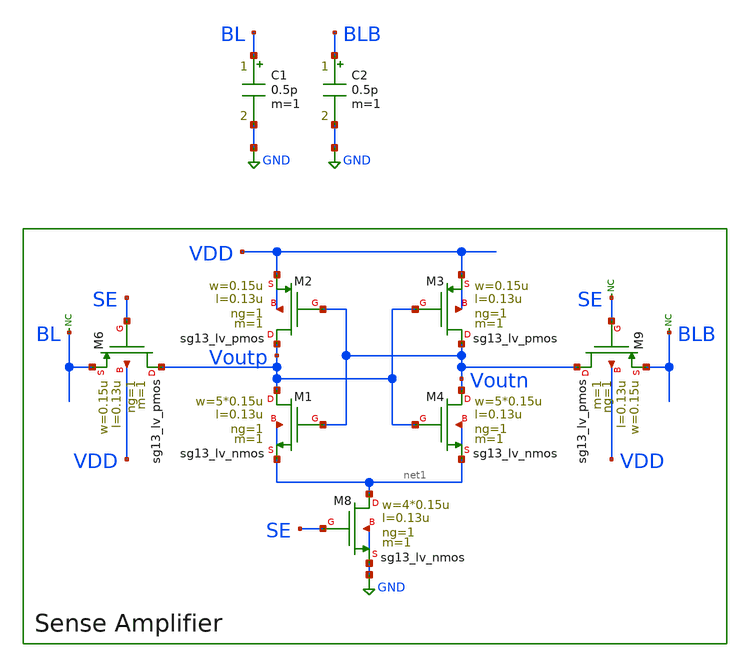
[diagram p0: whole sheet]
** sch_path: xschem/offset_voltage_tester/offset-voltage-tester.sch
**.subckt offset-voltage-tester
XM8 net1 SE GND GND sg13_lv_nmos w=4*0.15u l=0.13u ng=1 m=1 mm_ok=1
XM1 Voutp Voutn net1 net1 sg13_lv_nmos w=5*0.15u l=0.13u ng=1 m=1 mm_ok=1
XM3 Voutn Voutp VDD VDD sg13_lv_pmos w=0.15u l=0.13u ng=1 m=1 mm_ok=1
XM2 Voutp Voutn VDD VDD sg13_lv_pmos w=0.15u l=0.13u ng=1 m=1 mm_ok=1
XM4 Voutn Voutp net1 net1 sg13_lv_nmos w=5*0.15u l=0.13u ng=1 m=1 mm_ok=1
XM6 Voutp SE BL VDD sg13_lv_pmos w=0.15u l=0.13u ng=1 m=1 mm_ok=1
XM9 Voutn SE BLB VDD sg13_lv_pmos w=0.15u l=0.13u ng=1 m=1 mm_ok=1
* noconn SE
* noconn BLB
* noconn BL
C1 BL GND 0.5p m=1
C2 BLB GND 0.5p m=1
**** begin user architecture code



.lib cornerMOSlv.lib mos_tt_mismatch

.param mm_ok=1
.param mc_ok=1
.param temp=27

.param VDD=1.2
.param VCM=1.2
.param vind=0

.param TPER=10n
.param TSE_DLY=4n
.param TSE_W=3n
.param TR=100p
.param TF=100p
.param TEVAL=6.5n

VDD_S VDD 0 {VDD}
*VSE SE 0 {VDD}
* Force SE high
VSE SE 0 PULSE(0 {VDD} {TSE_DLY} {TR} {TF} {TSE_W} {TPER})
* SE Pulse:
* 0V -> VDD @ TSE_DLY
* Stays high for TSE_W
* Repeats every TPER

B_BLDRV BLDRV 0 V = {VCM + vind / 2}
B_BLBDRV BLBDRV 0 V = {VCM - vind / 2}

RBL BLDRV BL 50
RBLB BLBDRV BLB 50

.control

set noaskquit
set numdgt=10

let mc_runs = 3
let run = 0

set curplot = new
set scratch = $curplot
setplot $scratch

let vos_r_vec = unitvec(mc_runs)
let vos_f_vec = unitvec(mc_runs)
let indices = unitvec(mc_runs)

dowhile run < mc_runs
    source /foss/designs/sram-sense-amp/xschem/offset_voltage_tester/offset_voltage_tester.sp
    let indices[run] = run
    let run = run + 1
end

setscale indices
set wr_vecnames
wrdata vos_r.out vos_r_vec
wrdata vos_f.out vos_f_vec

write vos_results.raw

echo
print {$scratch}.vos_r_vec
print {$scratch}.vos_f_vec


*let vos_avg = (vos_r + vos_f) / 2
*let vos_diff = vos_r - vos_f

*echo 'vos_r = ' $&vos_r
*echo 'vos_f = ' $&vos_f
*echo 'diff  = ' $&vos_diff
.endc



**** end user architecture code
**.ends
.GLOBAL GND
.end
